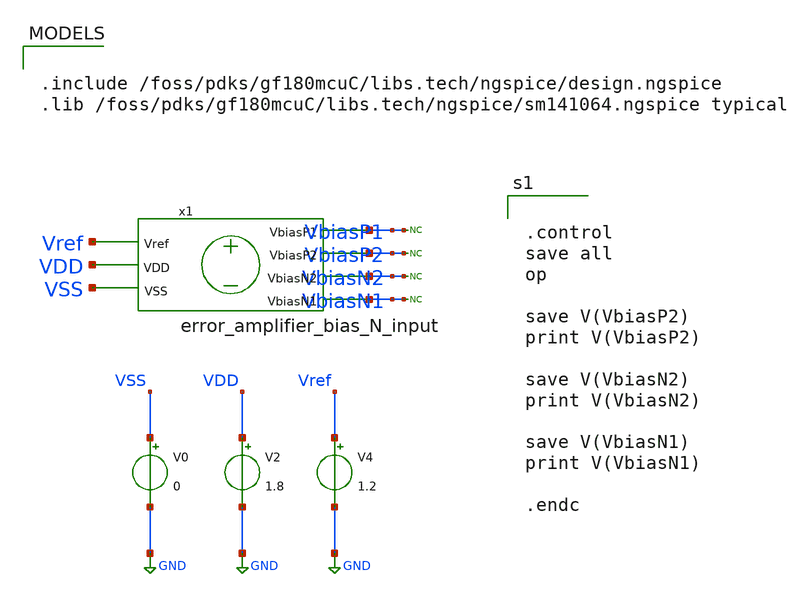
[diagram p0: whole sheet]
** sch_path: blocks/composite/folded_cascode/designs/gf180/error_amplifier_bias_N_input/xschem/error_amplifier_bias_OP.sch
**.subckt error_amplifier_bias_OP
V0 VSS GND 0
V2 VDD GND 1.8
V4 Vref GND 1.2
* noconn VbiasP2
* noconn VbiasN2
* noconn VbiasN1
x1 VbiasN1 VbiasN2 VbiasP2 VDD VSS Vref VbiasP1 error_amplifier_bias_N_input
* noconn VbiasP1
**** begin user architecture code

.include /foss/pdks/gf180mcuC/libs.tech/ngspice/design.ngspice
.lib /foss/pdks/gf180mcuC/libs.tech/ngspice/sm141064.ngspice typical



.control
save all
op

save V(VbiasP2)
print V(VbiasP2)

save V(VbiasN2)
print V(VbiasN2)

save V(VbiasN1)
print V(VbiasN1)

.endc


**** end user architecture code
**.ends

* expanding   symbol:  gf180/error_amplifier_bias_N_input/xschem/error_amplifier_bias_N_input.sym #
*+ of pins=7
** sym_path: blocks/composite/folded_cascode/designs/gf180/error_amplifier_bias_N_input/xschem/error_amplifier_bias_N_input.sym
** sch_path: blocks/composite/folded_cascode/designs/gf180/error_amplifier_bias_N_input/xschem/error_amplifier_bias_N_input.sch
.subckt error_amplifier_bias_N_input VbiasN1 VbiasN2 VbiasP2 VDD VSS Vref VbiasP1
*.ipin Vref
*.iopin VbiasN1
*.iopin VbiasN2
*.iopin VDD
*.iopin VbiasP2
*.iopin VSS
*.iopin VbiasP1
XM1 VbiasN2 VbiasN2 net2 VSS nfet_03v3 L=6u W=0.5u nf=1 ad='int((nf+1)/2) * W/nf * 0.18u' as='int((nf+2)/2) * W/nf * 0.18u'
+ pd='2*int((nf+1)/2) * (W/nf + 0.18u)' ps='2*int((nf+2)/2) * (W/nf + 0.18u)' nrd='0.18u / W' nrs='0.18u / W'
+ sa=0 sb=0 sd=0 m=1
XM2 VbiasP1 VbiasP1 VDD VDD pfet_03v3 L=2u W=0.5u nf=1 ad='int((nf+1)/2) * W/nf * 0.18u' as='int((nf+2)/2) * W/nf * 0.18u'
+ pd='2*int((nf+1)/2) * (W/nf + 0.18u)' ps='2*int((nf+2)/2) * (W/nf + 0.18u)' nrd='0.18u / W' nrs='0.18u / W'
+ sa=0 sb=0 sd=0 m=1
XM3 VbiasP1 Vref net1 VSS nfet_03v3 L=6u W=0.5u nf=1 ad='int((nf+1)/2) * W/nf * 0.18u' as='int((nf+2)/2) * W/nf * 0.18u'
+ pd='2*int((nf+1)/2) * (W/nf + 0.18u)' ps='2*int((nf+2)/2) * (W/nf + 0.18u)' nrd='0.18u / W' nrs='0.18u / W'
+ sa=0 sb=0 sd=0 m=1
XM4 VbiasN2 VbiasP1 VDD VDD pfet_03v3 L=2u W=0.5u nf=1 ad='int((nf+1)/2) * W/nf * 0.18u' as='int((nf+2)/2) * W/nf * 0.18u'
+ pd='2*int((nf+1)/2) * (W/nf + 0.18u)' ps='2*int((nf+2)/2) * (W/nf + 0.18u)' nrd='0.18u / W' nrs='0.18u / W'
+ sa=0 sb=0 sd=0 m=1
XM5 VbiasN1 VbiasP1 VDD VDD pfet_03v3 L=2u W=0.5u nf=1 ad='int((nf+1)/2) * W/nf * 0.18u' as='int((nf+2)/2) * W/nf * 0.18u'
+ pd='2*int((nf+1)/2) * (W/nf + 0.18u)' ps='2*int((nf+2)/2) * (W/nf + 0.18u)' nrd='0.18u / W' nrs='0.18u / W'
+ sa=0 sb=0 sd=0 m=1
XM6 net6 VbiasP2 VDD VDD pfet_03v3 L=2u W=0.5u nf=1 ad='int((nf+1)/2) * W/nf * 0.18u' as='int((nf+2)/2) * W/nf * 0.18u'
+ pd='2*int((nf+1)/2) * (W/nf + 0.18u)' ps='2*int((nf+2)/2) * (W/nf + 0.18u)' nrd='0.18u / W' nrs='0.18u / W'
+ sa=0 sb=0 sd=0 m=1
XM7 VbiasP2 VbiasP2 net6 VDD pfet_03v3 L=2u W=0.5u nf=1 ad='int((nf+1)/2) * W/nf * 0.18u' as='int((nf+2)/2) * W/nf * 0.18u'
+ pd='2*int((nf+1)/2) * (W/nf + 0.18u)' ps='2*int((nf+2)/2) * (W/nf + 0.18u)' nrd='0.18u / W' nrs='0.18u / W'
+ sa=0 sb=0 sd=0 m=1
XM8 net7 net8 VDD VDD pfet_03v3 L=2u W=0.5u nf=1 ad='int((nf+1)/2) * W/nf * 0.18u' as='int((nf+2)/2) * W/nf * 0.18u'
+ pd='2*int((nf+1)/2) * (W/nf + 0.18u)' ps='2*int((nf+2)/2) * (W/nf + 0.18u)' nrd='0.18u / W' nrs='0.18u / W'
+ sa=0 sb=0 sd=0 m=3
XM9 net8 VbiasP2 net7 VDD pfet_03v3 L=2u W=0.5u nf=1 ad='int((nf+1)/2) * W/nf * 0.18u' as='int((nf+2)/2) * W/nf * 0.18u'
+ pd='2*int((nf+1)/2) * (W/nf + 0.18u)' ps='2*int((nf+2)/2) * (W/nf + 0.18u)' nrd='0.18u / W' nrs='0.18u / W'
+ sa=0 sb=0 sd=0 m=2
XM10 net10 VbiasN1 VSS VSS nfet_03v3 L=6u W=0.5u nf=1 ad='int((nf+1)/2) * W/nf * 0.18u' as='int((nf+2)/2) * W/nf * 0.18u'
+ pd='2*int((nf+1)/2) * (W/nf + 0.18u)' ps='2*int((nf+2)/2) * (W/nf + 0.18u)' nrd='0.18u / W' nrs='0.18u / W'
+ sa=0 sb=0 sd=0 m=4
XM11 VbiasN1 VbiasN2 net3 VSS nfet_03v3 L=6u W=0.5u nf=1 ad='int((nf+1)/2) * W/nf * 0.18u' as='int((nf+2)/2) * W/nf * 0.18u'
+ pd='2*int((nf+1)/2) * (W/nf + 0.18u)' ps='2*int((nf+2)/2) * (W/nf + 0.18u)' nrd='0.18u / W' nrs='0.18u / W'
+ sa=0 sb=0 sd=0 m=5
XM12 VbiasP2 VbiasN2 net4 VSS nfet_03v3 L=6u W=0.5u nf=1 ad='int((nf+1)/2) * W/nf * 0.18u' as='int((nf+2)/2) * W/nf * 0.18u'
+ pd='2*int((nf+1)/2) * (W/nf + 0.18u)' ps='2*int((nf+2)/2) * (W/nf + 0.18u)' nrd='0.18u / W' nrs='0.18u / W'
+ sa=0 sb=0 sd=0 m=5
XM13 net8 VbiasN2 net9 VSS nfet_03v3 L=6u W=0.5u nf=1 ad='int((nf+1)/2) * W/nf * 0.18u' as='int((nf+2)/2) * W/nf * 0.18u'
+ pd='2*int((nf+1)/2) * (W/nf + 0.18u)' ps='2*int((nf+2)/2) * (W/nf + 0.18u)' nrd='0.18u / W' nrs='0.18u / W'
+ sa=0 sb=0 sd=0 m=5
XM14 net2 VbiasN2 VSS VSS nfet_03v3 L=6u W=0.5u nf=1 ad='int((nf+1)/2) * W/nf * 0.18u' as='int((nf+2)/2) * W/nf * 0.18u'
+ pd='2*int((nf+1)/2) * (W/nf + 0.18u)' ps='2*int((nf+2)/2) * (W/nf + 0.18u)' nrd='0.18u / W' nrs='0.18u / W'
+ sa=0 sb=0 sd=0 m=1
XM15 net3 VbiasN1 net11 VSS nfet_03v3 L=6u W=0.5u nf=1 ad='int((nf+1)/2) * W/nf * 0.18u' as='int((nf+2)/2) * W/nf * 0.18u'
+ pd='2*int((nf+1)/2) * (W/nf + 0.18u)' ps='2*int((nf+2)/2) * (W/nf + 0.18u)' nrd='0.18u / W' nrs='0.18u / W'
+ sa=0 sb=0 sd=0 m=4
XM16 net4 VbiasN1 net5 VSS nfet_03v3 L=6u W=0.5u nf=1 ad='int((nf+1)/2) * W/nf * 0.18u' as='int((nf+2)/2) * W/nf * 0.18u'
+ pd='2*int((nf+1)/2) * (W/nf + 0.18u)' ps='2*int((nf+2)/2) * (W/nf + 0.18u)' nrd='0.18u / W' nrs='0.18u / W'
+ sa=0 sb=0 sd=0 m=4
XM17 net9 VbiasN1 net10 VSS nfet_03v3 L=6u W=0.5u nf=1 ad='int((nf+1)/2) * W/nf * 0.18u' as='int((nf+2)/2) * W/nf * 0.18u'
+ pd='2*int((nf+1)/2) * (W/nf + 0.18u)' ps='2*int((nf+2)/2) * (W/nf + 0.18u)' nrd='0.18u / W' nrs='0.18u / W'
+ sa=0 sb=0 sd=0 m=4
XM18 net1 Vref VSS VSS nfet_03v3 L=6u W=0.5u nf=1 ad='int((nf+1)/2) * W/nf * 0.18u' as='int((nf+2)/2) * W/nf * 0.18u'
+ pd='2*int((nf+1)/2) * (W/nf + 0.18u)' ps='2*int((nf+2)/2) * (W/nf + 0.18u)' nrd='0.18u / W' nrs='0.18u / W'
+ sa=0 sb=0 sd=0 m=1
XM19 net5 VbiasN1 VSS VSS nfet_03v3 L=6u W=0.5u nf=1 ad='int((nf+1)/2) * W/nf * 0.18u' as='int((nf+2)/2) * W/nf * 0.18u'
+ pd='2*int((nf+1)/2) * (W/nf + 0.18u)' ps='2*int((nf+2)/2) * (W/nf + 0.18u)' nrd='0.18u / W' nrs='0.18u / W'
+ sa=0 sb=0 sd=0 m=4
XM20 net11 VbiasN1 VSS VSS nfet_03v3 L=6u W=0.5u nf=1 ad='int((nf+1)/2) * W/nf * 0.18u' as='int((nf+2)/2) * W/nf * 0.18u'
+ pd='2*int((nf+1)/2) * (W/nf + 0.18u)' ps='2*int((nf+2)/2) * (W/nf + 0.18u)' nrd='0.18u / W' nrs='0.18u / W'
+ sa=0 sb=0 sd=0 m=4
.ends

.GLOBAL GND
.end
